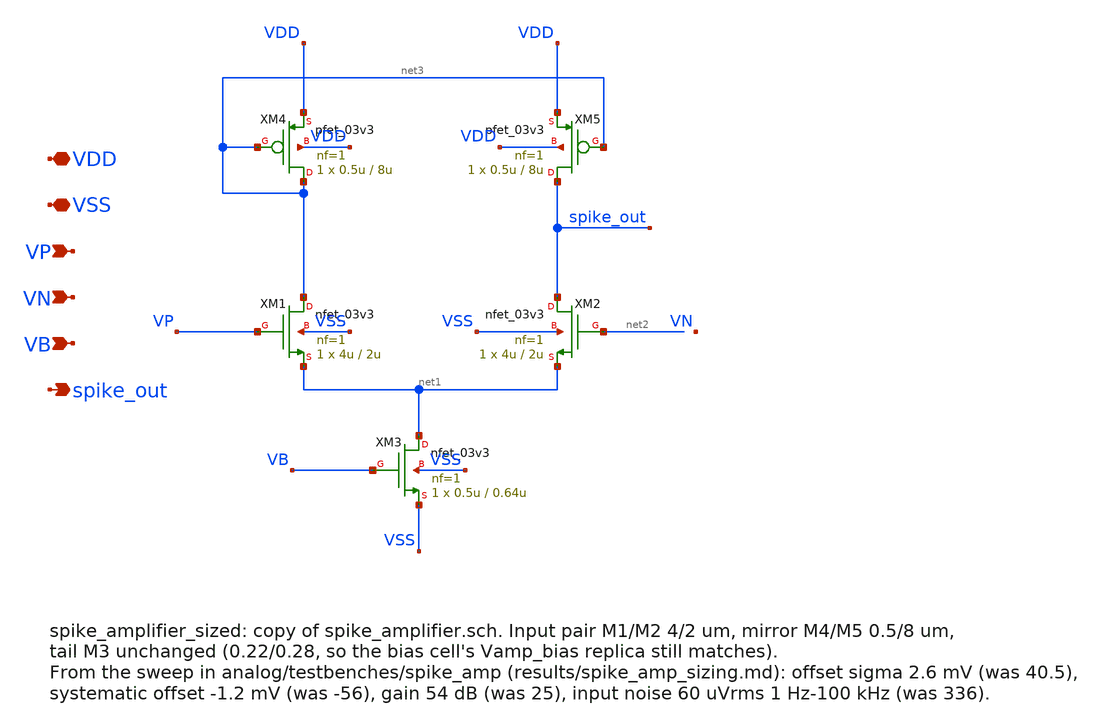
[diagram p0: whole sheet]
** sch_path: analog/neuron/spike_amplifier_sized.sch
**.subckt spike_amplifier_sized VDD VSS VP VN VB spike_out
*.iopin VDD
*.iopin VSS
*.ipin VP
*.ipin VN
*.ipin VB
*.opin spike_out
XM1 net3 VP net1 VSS nfet_03v3 L=2u W=4u nf=1 ad='int((nf+1)/2) * W/nf * 0.18u' as='int((nf+2)/2) * W/nf * 0.18u'
+ pd='2*int((nf+1)/2) * (W/nf + 0.18u)' ps='2*int((nf+2)/2) * (W/nf + 0.18u)' nrd='0.18u / W' nrs='0.18u / W'
+ sa=0 sb=0 sd=0 m=1
XM2 spike_out net2 net1 VSS nfet_03v3 L=2u W=4u nf=1 ad='int((nf+1)/2) * W/nf * 0.18u' as='int((nf+2)/2) * W/nf * 0.18u'
+ pd='2*int((nf+1)/2) * (W/nf + 0.18u)' ps='2*int((nf+2)/2) * (W/nf + 0.18u)' nrd='0.18u / W' nrs='0.18u / W'
+ sa=0 sb=0 sd=0 m=1
XM3 net1 VB VSS VSS nfet_03v3 L=0.64u W=0.5u nf=1 ad='int((nf+1)/2) * W/nf * 0.18u' as='int((nf+2)/2) * W/nf * 0.18u'
+ pd='2*int((nf+1)/2) * (W/nf + 0.18u)' ps='2*int((nf+2)/2) * (W/nf + 0.18u)' nrd='0.18u / W' nrs='0.18u / W'
+ sa=0 sb=0 sd=0 m=1
XM4 net3 net3 VDD VDD pfet_03v3 L=8u W=0.5u nf=1 ad='int((nf+1)/2) * W/nf * 0.18u' as='int((nf+2)/2) * W/nf * 0.18u'
+ pd='2*int((nf+1)/2) * (W/nf + 0.18u)' ps='2*int((nf+2)/2) * (W/nf + 0.18u)' nrd='0.18u / W' nrs='0.18u / W'
+ sa=0 sb=0 sd=0 m=1
XM5 spike_out net3 VDD VDD pfet_03v3 L=8u W=0.5u nf=1 ad='int((nf+1)/2) * W/nf * 0.18u' as='int((nf+2)/2) * W/nf * 0.18u'
+ pd='2*int((nf+1)/2) * (W/nf + 0.18u)' ps='2*int((nf+2)/2) * (W/nf + 0.18u)' nrd='0.18u / W' nrs='0.18u / W'
+ sa=0 sb=0 sd=0 m=1
**.ends
.end
